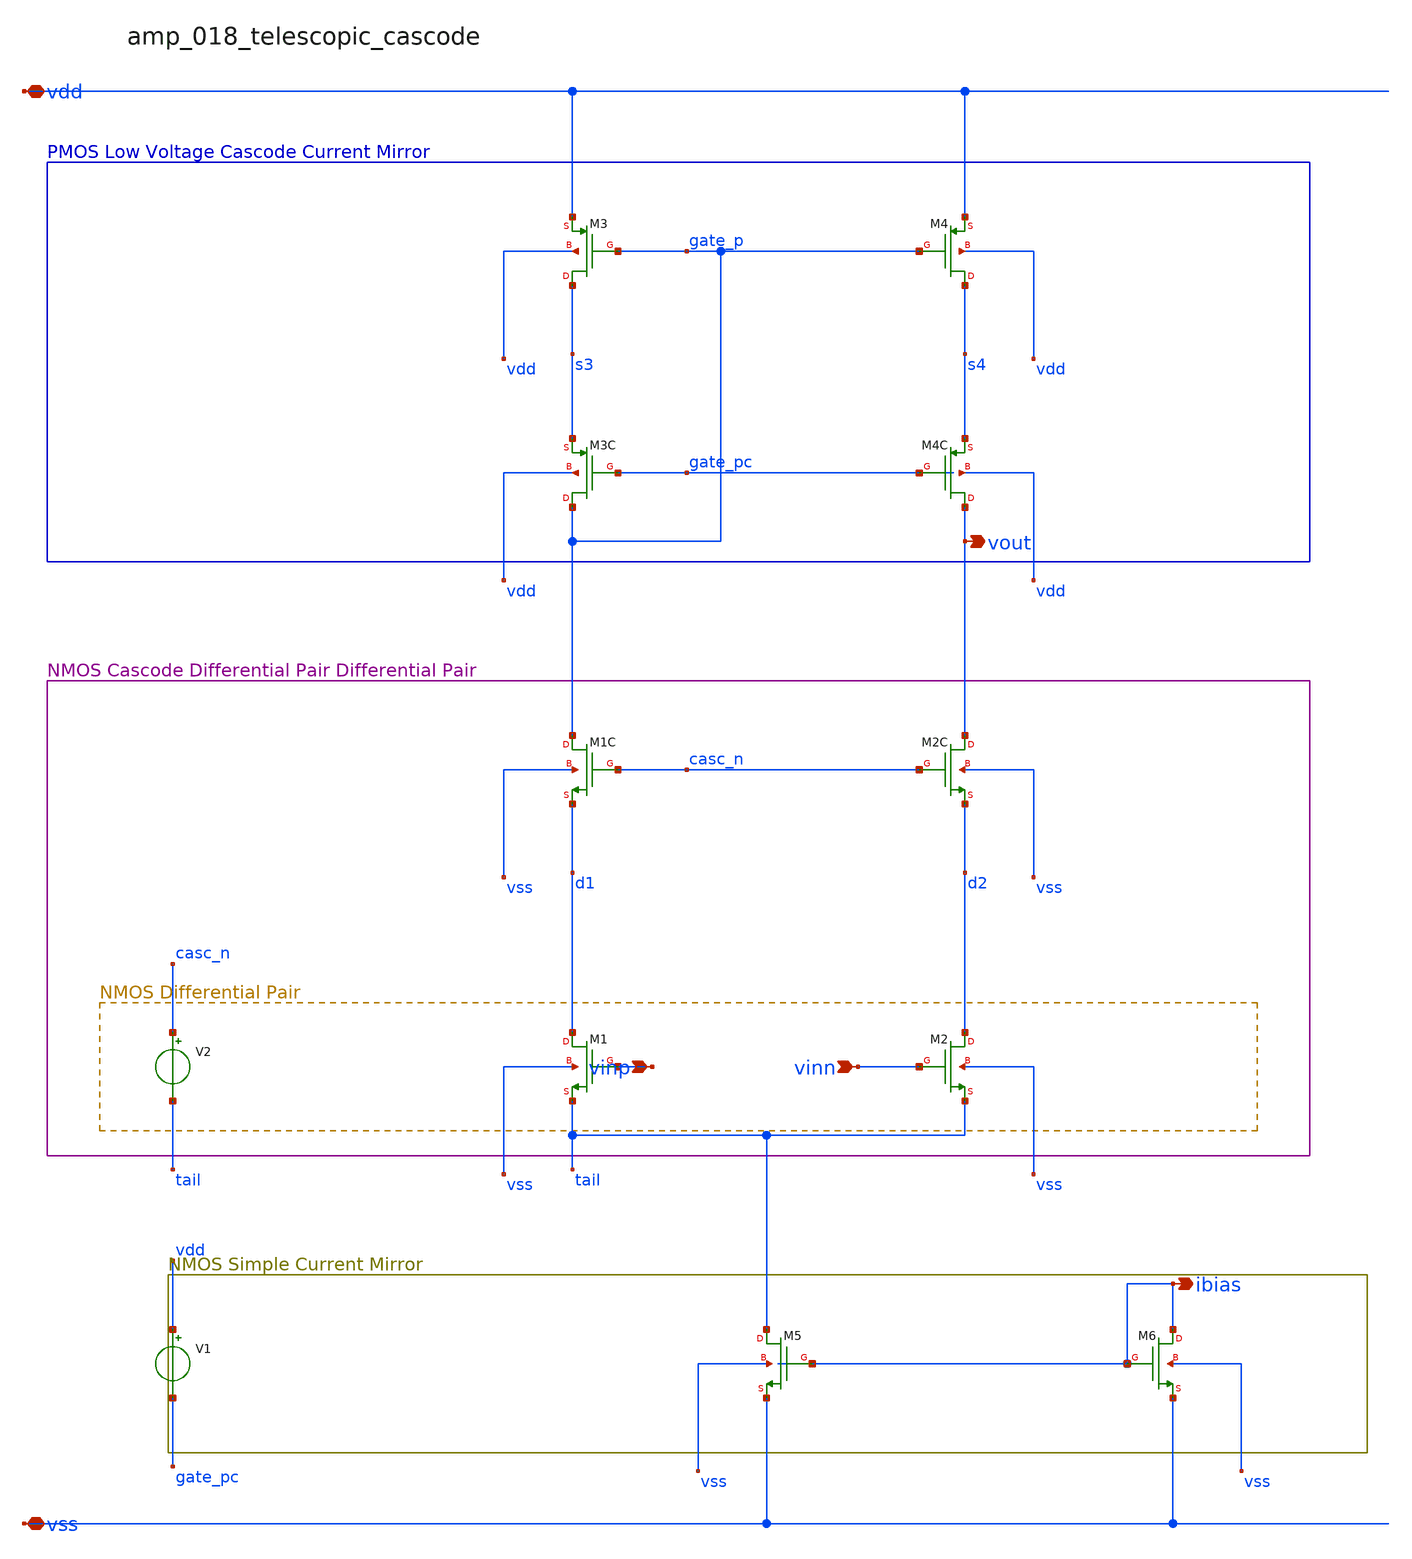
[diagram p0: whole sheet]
** sch_path: analog-db/raw/amp_018_telescopic_cascode/amp_018_telescopic_cascode_annotated.sch
**.subckt amp_018_telescopic_cascode_annotated vinp vinn vdd vss vout ibias
*.ipin vinp
*.ipin vinn
*.iopin vdd
*.iopin vss
*.opin vout
*.opin ibias
V1 vdd gate_pc x_dut_v_bias_2
V2 casc_n tail x_dut_v_bias_1
XM1 d1 vinp tail vss sg13_lv_nmos w=x_dut_xm1_w l=x_dut_xm1_l ng=1 m=x_dut_xm1_m
XM1C gate_p casc_n d1 vss sg13_lv_nmos w=x_dut_xm1c_w l=x_dut_xm1c_l ng=1 m=x_dut_xm1c_m
XM2 d2 vinn tail vss sg13_lv_nmos w=x_dut_xm2_w l=x_dut_xm2_l ng=1 m=x_dut_xm2_m
XM2C vout casc_n d2 vss sg13_lv_nmos w=x_dut_xm2c_w l=x_dut_xm2c_l ng=1 m=x_dut_xm2c_m
XM3 s3 gate_p vdd vdd sg13_lv_pmos w=x_dut_xm3_w l=x_dut_xm3_l ng=1 m=x_dut_xm3_m
XM3C gate_p gate_pc s3 vdd sg13_lv_pmos w=x_dut_xm3c_w l=x_dut_xm3c_l ng=1 m=x_dut_xm3c_m
XM4 s4 gate_p vdd vdd sg13_lv_pmos w=x_dut_xm4_w l=x_dut_xm4_l ng=1 m=x_dut_xm4_m
XM4C vout gate_pc s4 vdd sg13_lv_pmos w=x_dut_xm4c_w l=x_dut_xm4c_l ng=1 m=x_dut_xm4c_m
XM5 tail ibias vss vss sg13_lv_nmos w=x_dut_xm5_w l=x_dut_xm5_l ng=x_dut_xm5_ng m=x_dut_xm5_m
XM6 ibias ibias vss vss sg13_lv_nmos w=x_dut_xm6_w l=x_dut_xm6_l ng=1 m=x_dut_xm6_m
**.ends
.end
